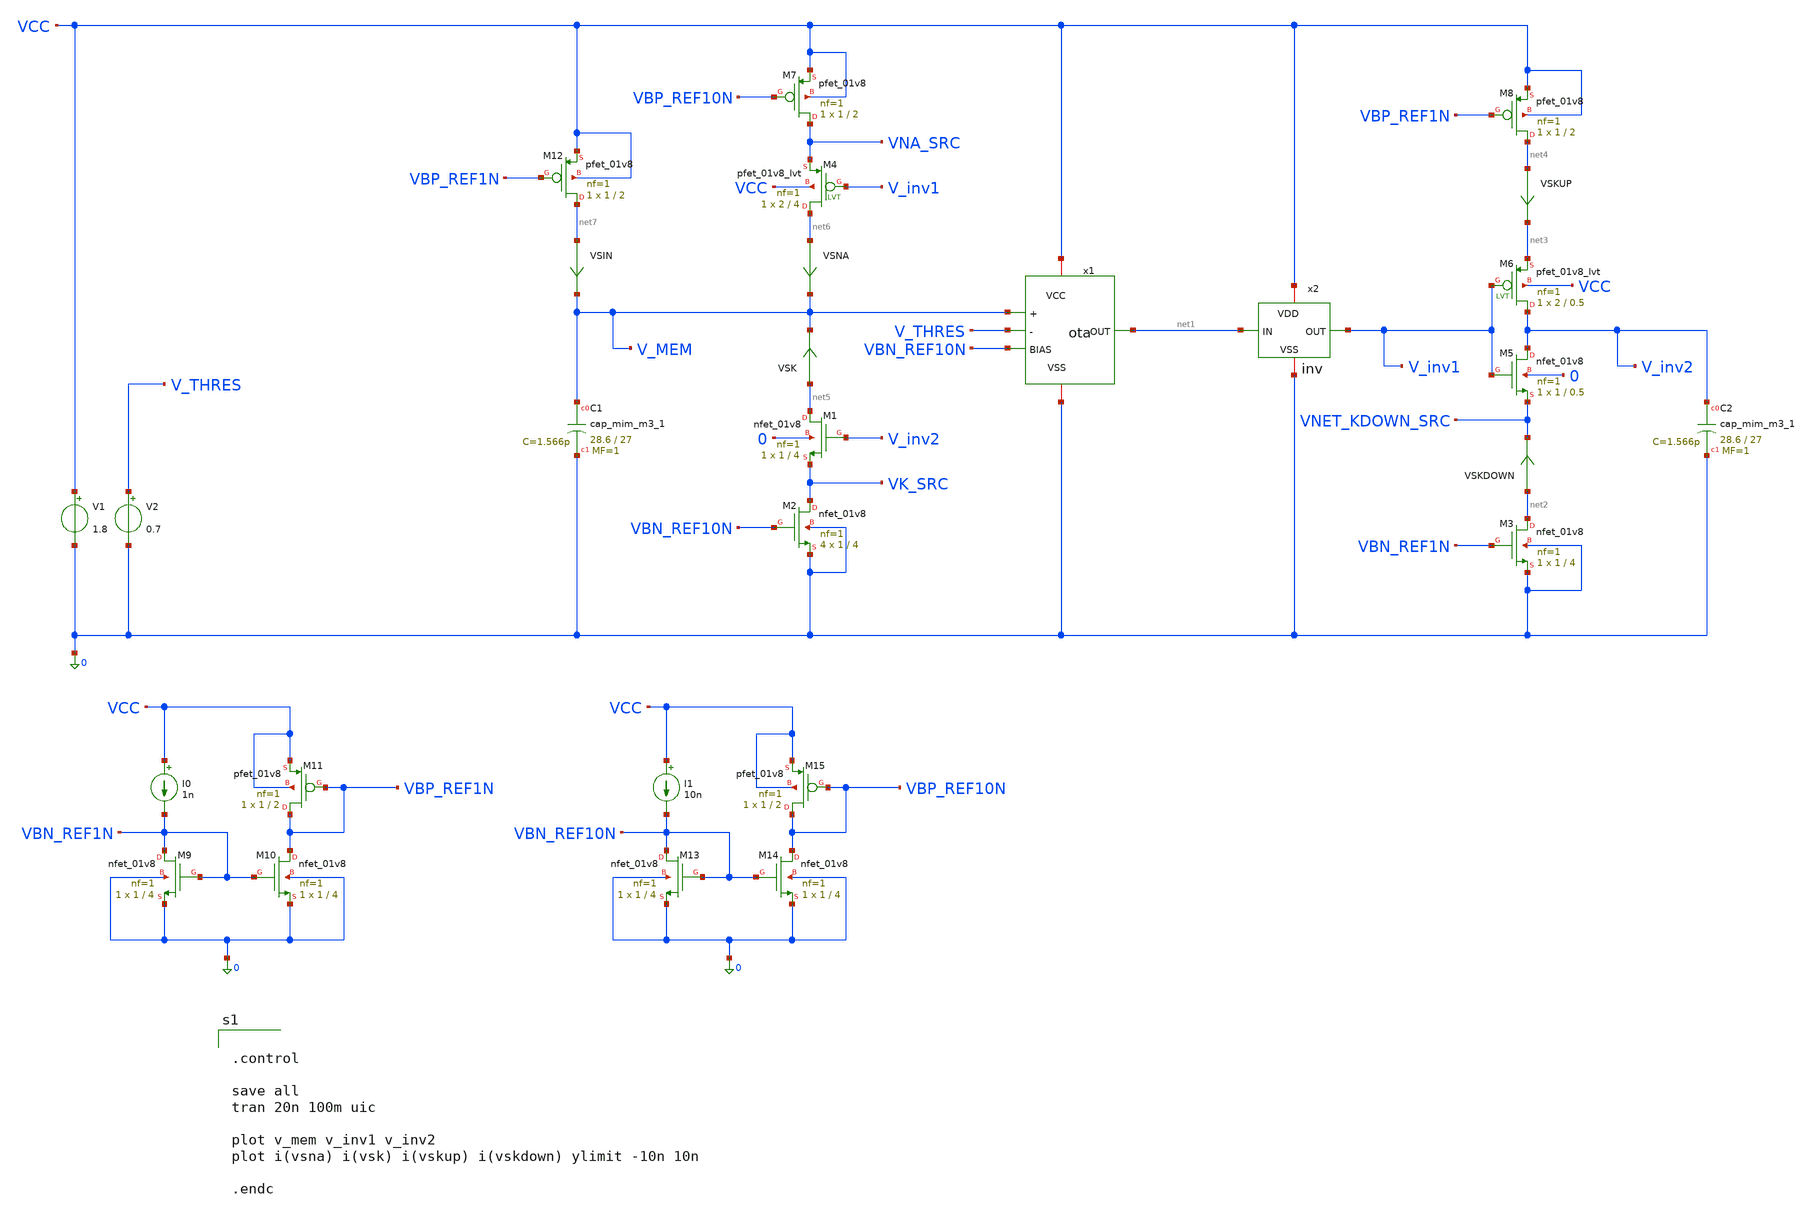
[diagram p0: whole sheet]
** sch_path: schem/vamp_if_neuron.sch
**.subckt vamp_if_neuron
x1 VCC net1 0 VBN_REF10N V_MEM V_THRES ota
x2 VCC net1 V_inv1 0 inv
XC1 V_MEM 0 sky130_fd_pr__cap_mim_m3_1 W=28.6 L=27 MF=1 m=1
XM1 net5 V_inv2 VK_SRC 0 sky130_fd_pr__nfet_01v8 L=4 W=1 nf=1 ad='int((1 + 1)/2) * 1 / 1 * 0.29' as='int((1 + 2)/2) * 1 / 1 * 0.29'
+ pd='2*int((1 + 1)/2) * (1 / 1 + 0.29)' ps='2*int((1 + 2)/2) * (1 / 1 + 0.29)' nrd='0.29 / 1 ' nrs='0.29 / 1 '
+ sa=0 sb=0 sd=0 mult=1 m=1
V1 VCC 0 1.8
V2 V_THRES 0 0.7
XM5 V_inv2 V_inv1 VNET_KDOWN_SRC 0 sky130_fd_pr__nfet_01v8 L=0.5 W=1 nf=1 ad='int((1 + 1)/2) * 1 / 1 * 0.29'
+ as='int((1 + 2)/2) * 1 / 1 * 0.29' pd='2*int((1 + 1)/2) * (1 / 1 + 0.29)' ps='2*int((1 + 2)/2) * (1 / 1 + 0.29)'
+ nrd='0.29 / 1 ' nrs='0.29 / 1 ' sa=0 sb=0 sd=0 mult=1 m=1
XM6 V_inv2 V_inv1 net3 VCC sky130_fd_pr__pfet_01v8_lvt L=0.5 W=2 nf=1 ad='int((1 + 1)/2) * 2 / 1 * 0.29'
+ as='int((1 + 2)/2) * 2 / 1 * 0.29' pd='2*int((1 + 1)/2) * (2 / 1 + 0.29)' ps='2*int((1 + 2)/2) * (2 / 1 + 0.29)'
+ nrd='0.29 / 2 ' nrs='0.29 / 2 ' sa=0 sb=0 sd=0 mult=1 m=1
XC2 V_inv2 0 sky130_fd_pr__cap_mim_m3_1 W=28.6 L=27 MF=1 m=1
VSNA net6 V_MEM 0
.save i(vsna)
VSKUP net4 net3 0
.save i(vskup)
VSK net5 V_MEM 0
.save i(vsk)
VSKDOWN net2 VNET_KDOWN_SRC 0
.save i(vskdown)
I0 VCC VBN_REF1N 1n
XM9 VBN_REF1N VBN_REF1N 0 0 sky130_fd_pr__nfet_01v8 L=4 W=1 nf=1 ad='int((1 + 1)/2) * 1 / 1 * 0.29' as='int((1 + 2)/2) * 1 / 1 * 0.29'
+ pd='2*int((1 + 1)/2) * (1 / 1 + 0.29)' ps='2*int((1 + 2)/2) * (1 / 1 + 0.29)' nrd='0.29 / 1 ' nrs='0.29 / 1 '
+ sa=0 sb=0 sd=0 mult=1 m=1
XM10 VBP_REF1N VBN_REF1N 0 0 sky130_fd_pr__nfet_01v8 L=4 W=1 nf=1 ad='int((1 + 1)/2) * 1 / 1 * 0.29'
+ as='int((1 + 2)/2) * 1 / 1 * 0.29' pd='2*int((1 + 1)/2) * (1 / 1 + 0.29)' ps='2*int((1 + 2)/2) * (1 / 1 + 0.29)'
+ nrd='0.29 / 1 ' nrs='0.29 / 1 ' sa=0 sb=0 sd=0 mult=1 m=1
I1 VCC VBN_REF10N 10n
XM13 VBN_REF10N VBN_REF10N 0 0 sky130_fd_pr__nfet_01v8 L=4 W=1 nf=1 ad='int((1 + 1)/2) * 1 / 1 * 0.29'
+ as='int((1 + 2)/2) * 1 / 1 * 0.29' pd='2*int((1 + 1)/2) * (1 / 1 + 0.29)' ps='2*int((1 + 2)/2) * (1 / 1 + 0.29)'
+ nrd='0.29 / 1 ' nrs='0.29 / 1 ' sa=0 sb=0 sd=0 mult=1 m=1
XM14 VBP_REF10N VBN_REF10N 0 0 sky130_fd_pr__nfet_01v8 L=4 W=1 nf=1 ad='int((1 + 1)/2) * 1 / 1 * 0.29'
+ as='int((1 + 2)/2) * 1 / 1 * 0.29' pd='2*int((1 + 1)/2) * (1 / 1 + 0.29)' ps='2*int((1 + 2)/2) * (1 / 1 + 0.29)'
+ nrd='0.29 / 1 ' nrs='0.29 / 1 ' sa=0 sb=0 sd=0 mult=1 m=1
XM11 VBP_REF1N VBP_REF1N VCC VCC sky130_fd_pr__pfet_01v8 L=2 W=1 nf=1 ad='int((1 + 1)/2) * 1 / 1 * 0.29'
+ as='int((1 + 2)/2) * 1 / 1 * 0.29' pd='2*int((1 + 1)/2) * (1 / 1 + 0.29)' ps='2*int((1 + 2)/2) * (1 / 1 + 0.29)'
+ nrd='0.29 / 1 ' nrs='0.29 / 1 ' sa=0 sb=0 sd=0 mult=1 m=1
XM15 VBP_REF10N VBP_REF10N VCC VCC sky130_fd_pr__pfet_01v8 L=2 W=1 nf=1 ad='int((1 + 1)/2) * 1 / 1 * 0.29'
+ as='int((1 + 2)/2) * 1 / 1 * 0.29' pd='2*int((1 + 1)/2) * (1 / 1 + 0.29)' ps='2*int((1 + 2)/2) * (1 / 1 + 0.29)'
+ nrd='0.29 / 1 ' nrs='0.29 / 1 ' sa=0 sb=0 sd=0 mult=1 m=1
XM2 VK_SRC VBN_REF10N 0 0 sky130_fd_pr__nfet_01v8 L=4 W=1 nf=1 ad='int((1 + 1)/2) * 1 / 1 * 0.29' as='int((1 + 2)/2) * 1 / 1 * 0.29'
+ pd='2*int((1 + 1)/2) * (1 / 1 + 0.29)' ps='2*int((1 + 2)/2) * (1 / 1 + 0.29)' nrd='0.29 / 1 ' nrs='0.29 / 1 '
+ sa=0 sb=0 sd=0 mult=4 m=4
XM3 net2 VBN_REF1N 0 0 sky130_fd_pr__nfet_01v8 L=4 W=1 nf=1 ad='int((1 + 1)/2) * 1 / 1 * 0.29' as='int((1 + 2)/2) * 1 / 1 * 0.29'
+ pd='2*int((1 + 1)/2) * (1 / 1 + 0.29)' ps='2*int((1 + 2)/2) * (1 / 1 + 0.29)' nrd='0.29 / 1 ' nrs='0.29 / 1 '
+ sa=0 sb=0 sd=0 mult=1 m=1
XM7 VNA_SRC VBP_REF10N VCC VCC sky130_fd_pr__pfet_01v8 L=2 W=1 nf=1 ad='int((1 + 1)/2) * 1 / 1 * 0.29'
+ as='int((1 + 2)/2) * 1 / 1 * 0.29' pd='2*int((1 + 1)/2) * (1 / 1 + 0.29)' ps='2*int((1 + 2)/2) * (1 / 1 + 0.29)'
+ nrd='0.29 / 1 ' nrs='0.29 / 1 ' sa=0 sb=0 sd=0 mult=1 m=1
XM8 net4 VBP_REF1N VCC VCC sky130_fd_pr__pfet_01v8 L=2 W=1 nf=1 ad='int((1 + 1)/2) * 1 / 1 * 0.29' as='int((1 + 2)/2) * 1 / 1 * 0.29'
+ pd='2*int((1 + 1)/2) * (1 / 1 + 0.29)' ps='2*int((1 + 2)/2) * (1 / 1 + 0.29)' nrd='0.29 / 1 ' nrs='0.29 / 1 '
+ sa=0 sb=0 sd=0 mult=1 m=1
XM4 net6 V_inv1 VNA_SRC VCC sky130_fd_pr__pfet_01v8_lvt L=4 W=2 nf=1 ad='int((1 + 1)/2) * 2 / 1 * 0.29'
+ as='int((1 + 2)/2) * 2 / 1 * 0.29' pd='2*int((1 + 1)/2) * (2 / 1 + 0.29)' ps='2*int((1 + 2)/2) * (2 / 1 + 0.29)'
+ nrd='0.29 / 2 ' nrs='0.29 / 2 ' sa=0 sb=0 sd=0 mult=1 m=1
XM12 net7 VBP_REF1N VCC VCC sky130_fd_pr__pfet_01v8 L=2 W=1 nf=1 ad='int((1 + 1)/2) * 1 / 1 * 0.29' as='int((1 + 2)/2) * 1 / 1 * 0.29'
+ pd='2*int((1 + 1)/2) * (1 / 1 + 0.29)' ps='2*int((1 + 2)/2) * (1 / 1 + 0.29)' nrd='0.29 / 1 ' nrs='0.29 / 1 '
+ sa=0 sb=0 sd=0 mult=1 m=1
VSIN net7 V_MEM 0
.save i(vsin)
**** begin user architecture code

** opencircuitdesign pdks install
.lib $::SKYWATER_MODELS/sky130.lib.spice tt



.control

save all
tran 20n 100m uic

plot v_mem v_inv1 v_inv2
plot i(vsna) i(vsk) i(vskup) i(vskdown) ylimit -10n 10n

.endc


**** end user architecture code
**.ends

* expanding   symbol:  /foss/designs/ttsky-26c-voltage-amplifier-neuron/schem/ota/ota.sym # of
*+ pins=6
** sym_path: schem/ota/ota.sym
** sch_path: schem/ota/ota.sch
.subckt ota VCC OUT VSS BIAS + -
*.ipin BIAS
*.ipin +
*.ipin -
*.opin OUT
*.iopin VCC
*.iopin VSS
XM1 VSRC + VBOT VSS sky130_fd_pr__nfet_01v8 L=0.5 W=1 nf=1 ad='int((1 + 1)/2) * 1 / 1 * 0.29' as='int((1 + 2)/2) * 1 / 1 * 0.29'
+ pd='2*int((1 + 1)/2) * (1 / 1 + 0.29)' ps='2*int((1 + 2)/2) * (1 / 1 + 0.29)' nrd='0.29 / 1 ' nrs='0.29 / 1 '
+ sa=0 sb=0 sd=0 mult=1 m=1
XM2 OUT - VBOT VSS sky130_fd_pr__nfet_01v8 L=0.5 W=1 nf=1 ad='int((1 + 1)/2) * 1 / 1 * 0.29' as='int((1 + 2)/2) * 1 / 1 * 0.29'
+ pd='2*int((1 + 1)/2) * (1 / 1 + 0.29)' ps='2*int((1 + 2)/2) * (1 / 1 + 0.29)' nrd='0.29 / 1 ' nrs='0.29 / 1 '
+ sa=0 sb=0 sd=0 mult=1 m=1
XM3 VSRC VSRC VCC VCC sky130_fd_pr__pfet_01v8_lvt L=0.5 W=2 nf=1 ad='int((1 + 1)/2) * 2 / 1 * 0.29' as='int((1 + 2)/2) * 2 / 1 * 0.29'
+ pd='2*int((1 + 1)/2) * (2 / 1 + 0.29)' ps='2*int((1 + 2)/2) * (2 / 1 + 0.29)' nrd='0.29 / 2 ' nrs='0.29 / 2 '
+ sa=0 sb=0 sd=0 mult=1 m=1
XM4 OUT VSRC VCC VCC sky130_fd_pr__pfet_01v8_lvt L=0.5 W=2 nf=1 ad='int((1 + 1)/2) * 2 / 1 * 0.29' as='int((1 + 2)/2) * 2 / 1 * 0.29'
+ pd='2*int((1 + 1)/2) * (2 / 1 + 0.29)' ps='2*int((1 + 2)/2) * (2 / 1 + 0.29)' nrd='0.29 / 2 ' nrs='0.29 / 2 '
+ sa=0 sb=0 sd=0 mult=1 m=1
XM5 VBOT BIAS VSS VSS sky130_fd_pr__nfet_01v8 L=1 W=1 nf=1 ad='int((1 + 1)/2) * 1 / 1 * 0.29' as='int((1 + 2)/2) * 1 / 1 * 0.29'
+ pd='2*int((1 + 1)/2) * (1 / 1 + 0.29)' ps='2*int((1 + 2)/2) * (1 / 1 + 0.29)' nrd='0.29 / 1 ' nrs='0.29 / 1 '
+ sa=0 sb=0 sd=0 mult=2 m=2
.ends


* expanding   symbol:  /foss/designs/ttsky-26c-voltage-amplifier-neuron/schem/inv/inv.sym # of
*+ pins=4
** sym_path: schem/inv/inv.sym
** sch_path: schem/inv/inv.sch
.subckt inv VDD IN OUT VSS
*.ipin IN
*.iopin VDD
*.iopin VSS
*.opin OUT
XM1 OUT IN VSS VSS sky130_fd_pr__nfet_01v8 L=0.5 W=1 nf=1 ad='int((1 + 1)/2) * 1 / 1 * 0.29' as='int((1 + 2)/2) * 1 / 1 * 0.29'
+ pd='2*int((1 + 1)/2) * (1 / 1 + 0.29)' ps='2*int((1 + 2)/2) * (1 / 1 + 0.29)' nrd='0.29 / 1 ' nrs='0.29 / 1 '
+ sa=0 sb=0 sd=0 mult=1 m=1
XM2 OUT IN VDD VDD sky130_fd_pr__pfet_01v8_lvt L=0.5 W=2 nf=1 ad='int((1 + 1)/2) * 2 / 1 * 0.29' as='int((1 + 2)/2) * 2 / 1 * 0.29'
+ pd='2*int((1 + 1)/2) * (2 / 1 + 0.29)' ps='2*int((1 + 2)/2) * (2 / 1 + 0.29)' nrd='0.29 / 2 ' nrs='0.29 / 2 '
+ sa=0 sb=0 sd=0 mult=1 m=1
.ends

.end
